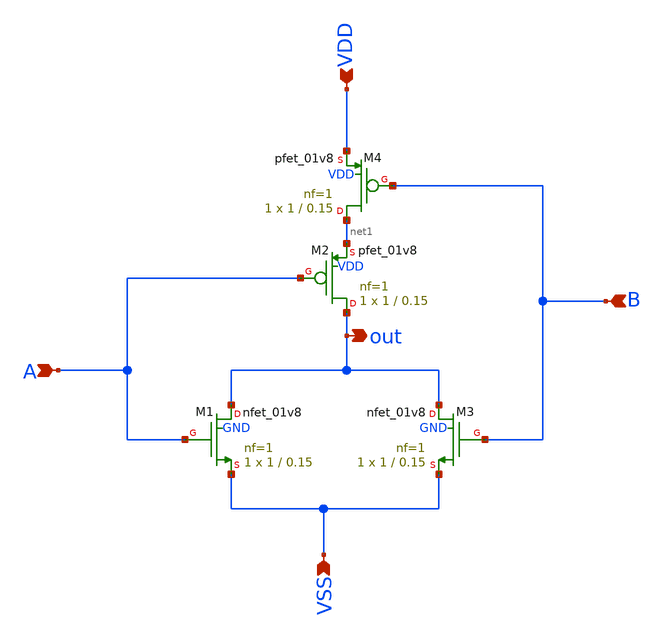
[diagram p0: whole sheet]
** sch_path: 2_bit_current_steering_DAC/nor.sch
**.subckt nor A B VDD VSS out
*.ipin A
*.ipin B
*.ipin VDD
*.ipin VSS
*.opin out
XM1 out A VSS GND sky130_fd_pr__nfet_01v8 L=0.15 W=1 nf=1 ad='int((1 + 1)/2) * 1 / 1 * 0.29' as='int((1 + 2)/2) * 1 / 1 * 0.29'
+ pd='2*int((1 + 1)/2) * (1 / 1 + 0.29)' ps='2*int((1 + 2)/2) * (1 / 1 + 0.29)' nrd='0.29 / 1 ' nrs='0.29 / 1 '
+ sa=0 sb=0 sd=0 mult=1 m=1
XM3 out B VSS GND sky130_fd_pr__nfet_01v8 L=0.15 W=1 nf=1 ad='int((1 + 1)/2) * 1 / 1 * 0.29' as='int((1 + 2)/2) * 1 / 1 * 0.29'
+ pd='2*int((1 + 1)/2) * (1 / 1 + 0.29)' ps='2*int((1 + 2)/2) * (1 / 1 + 0.29)' nrd='0.29 / 1 ' nrs='0.29 / 1 '
+ sa=0 sb=0 sd=0 mult=1 m=1
XM2 out A net1 VDD sky130_fd_pr__pfet_01v8 L=0.15 W=1 nf=1 ad='int((1 + 1)/2) * 1 / 1 * 0.29' as='int((1 + 2)/2) * 1 / 1 * 0.29'
+ pd='2*int((1 + 1)/2) * (1 / 1 + 0.29)' ps='2*int((1 + 2)/2) * (1 / 1 + 0.29)' nrd='0.29 / 1 ' nrs='0.29 / 1 '
+ sa=0 sb=0 sd=0 mult=1 m=1
XM4 net1 B VDD VDD sky130_fd_pr__pfet_01v8 L=0.15 W=1 nf=1 ad='int((1 + 1)/2) * 1 / 1 * 0.29' as='int((1 + 2)/2) * 1 / 1 * 0.29'
+ pd='2*int((1 + 1)/2) * (1 / 1 + 0.29)' ps='2*int((1 + 2)/2) * (1 / 1 + 0.29)' nrd='0.29 / 1 ' nrs='0.29 / 1 '
+ sa=0 sb=0 sd=0 mult=1 m=1
**.ends
.end
